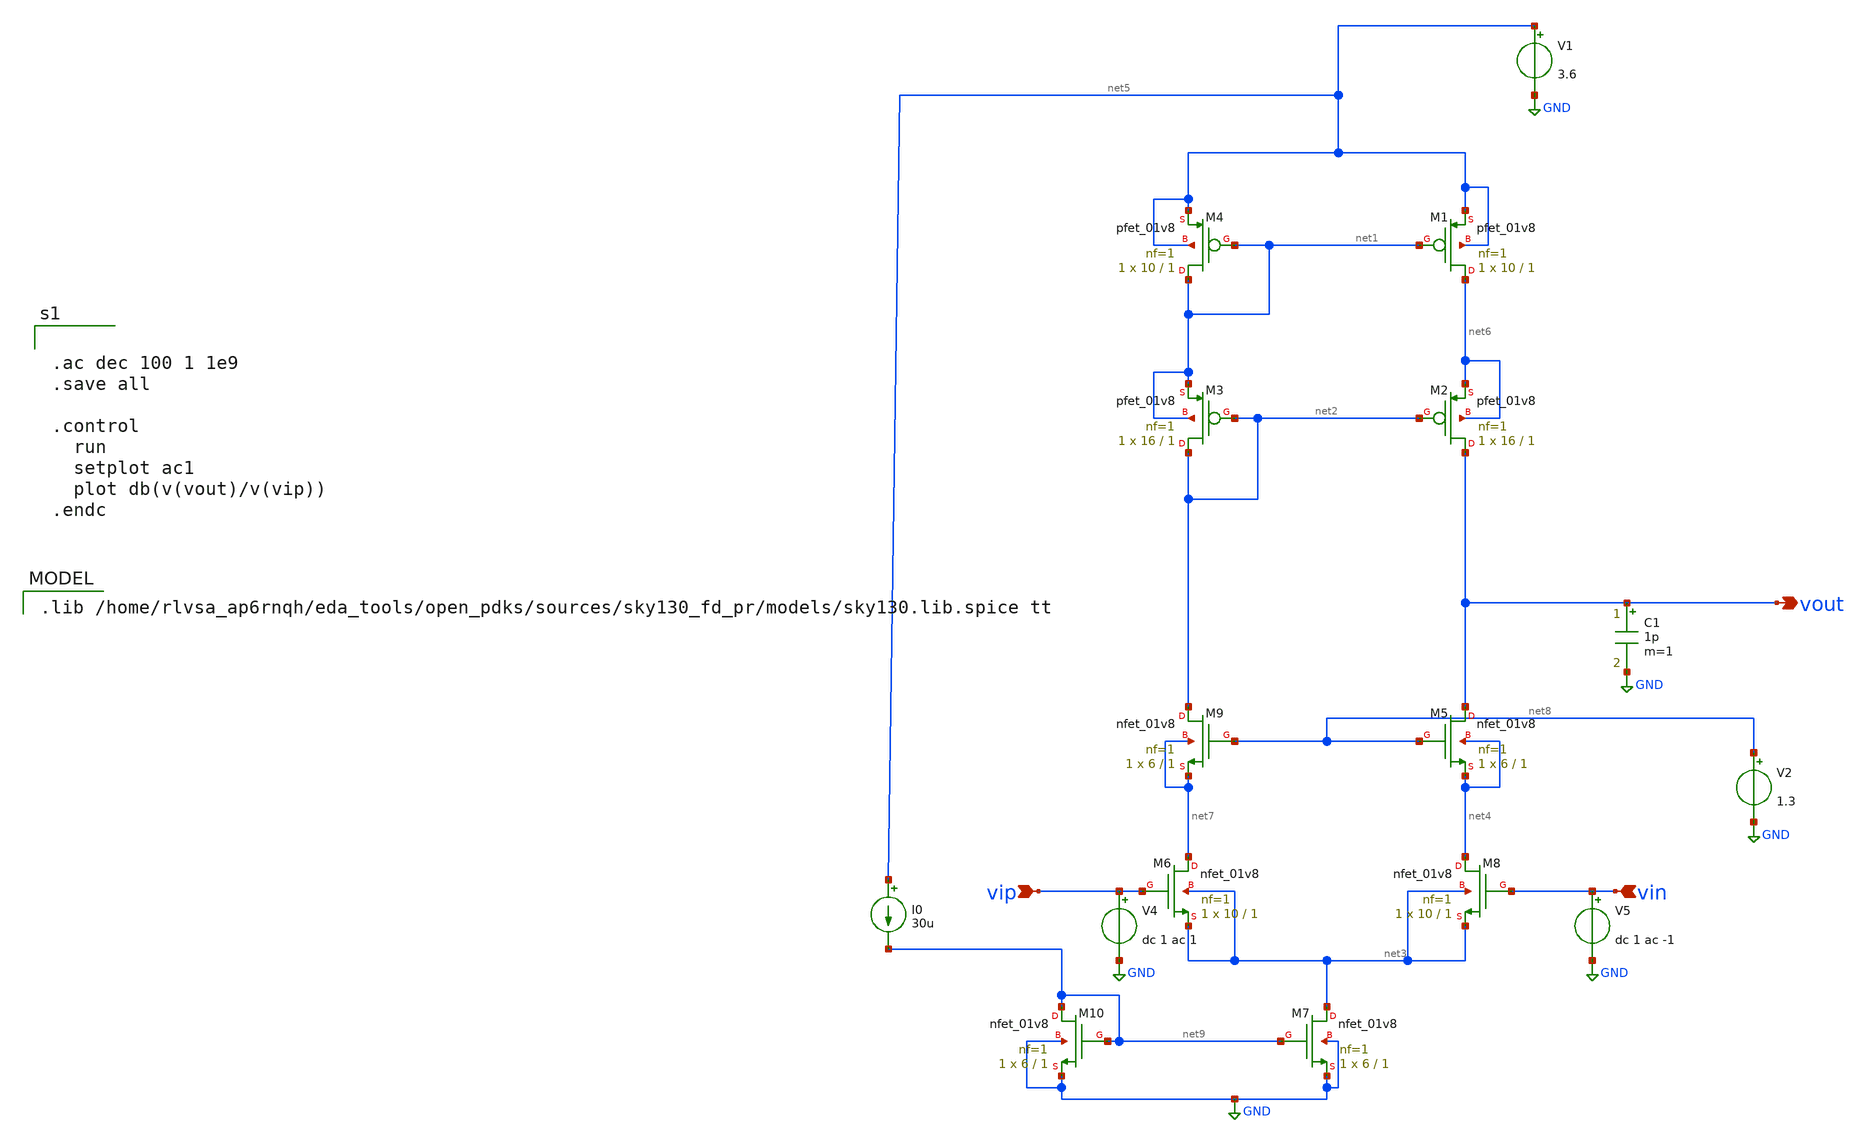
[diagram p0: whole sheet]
** sch_path: Telscopic_Opamp/9T_schematic.sch
**.subckt 9T_schematic vout vip vin
*.opin vout
*.ipin vip
*.ipin vin
V1 net5 GND 3.6
C1 vout GND 1p m=1
V2 net8 GND 1.3
V4 vip GND dc 1 ac 1
V5 vin GND dc 1 ac -1
I0 net5 net9 30u
XM5 vout net8 net4 net4 sky130_fd_pr__nfet_01v8 L=1 W=6 nf=1 ad='int((1 + 1)/2) * 6 / 1 * 0.29' as='int((1 + 2)/2) * 6 / 1 * 0.29'
+ pd='2*int((1 + 1)/2) * (6 / 1 + 0.29)' ps='2*int((1 + 2)/2) * (6 / 1 + 0.29)' nrd='0.29 / 6 ' nrs='0.29 / 6 '
+ sa=0 sb=0 sd=0 mult=1 m=1
XM6 net7 vip net3 net3 sky130_fd_pr__nfet_01v8 L=1 W=10 nf=1 ad='int((1 + 1)/2) * 10 / 1 * 0.29' as='int((1 + 2)/2) * 10 / 1 * 0.29'
+ pd='2*int((1 + 1)/2) * (10 / 1 + 0.29)' ps='2*int((1 + 2)/2) * (10 / 1 + 0.29)' nrd='0.29 / 10 ' nrs='0.29 / 10 '
+ sa=0 sb=0 sd=0 mult=1 m=1
XM7 net3 net9 GND GND sky130_fd_pr__nfet_01v8 L=1 W=6 nf=1 ad='int((1 + 1)/2) * 6 / 1 * 0.29' as='int((1 + 2)/2) * 6 / 1 * 0.29'
+ pd='2*int((1 + 1)/2) * (6 / 1 + 0.29)' ps='2*int((1 + 2)/2) * (6 / 1 + 0.29)' nrd='0.29 / 6 ' nrs='0.29 / 6 '
+ sa=0 sb=0 sd=0 mult=1 m=1
XM8 net4 vin net3 net3 sky130_fd_pr__nfet_01v8 L=1 W=10 nf=1 ad='int((1 + 1)/2) * 10 / 1 * 0.29' as='int((1 + 2)/2) * 10 / 1 * 0.29'
+ pd='2*int((1 + 1)/2) * (10 / 1 + 0.29)' ps='2*int((1 + 2)/2) * (10 / 1 + 0.29)' nrd='0.29 / 10 ' nrs='0.29 / 10 '
+ sa=0 sb=0 sd=0 mult=1 m=1
XM9 net2 net8 net7 net7 sky130_fd_pr__nfet_01v8 L=1 W=6 nf=1 ad='int((1 + 1)/2) * 6 / 1 * 0.29' as='int((1 + 2)/2) * 6 / 1 * 0.29'
+ pd='2*int((1 + 1)/2) * (6 / 1 + 0.29)' ps='2*int((1 + 2)/2) * (6 / 1 + 0.29)' nrd='0.29 / 6 ' nrs='0.29 / 6 '
+ sa=0 sb=0 sd=0 mult=1 m=1
XM10 net9 net9 GND GND sky130_fd_pr__nfet_01v8 L=1 W=6 nf=1 ad='int((1 + 1)/2) * 6 / 1 * 0.29' as='int((1 + 2)/2) * 6 / 1 * 0.29'
+ pd='2*int((1 + 1)/2) * (6 / 1 + 0.29)' ps='2*int((1 + 2)/2) * (6 / 1 + 0.29)' nrd='0.29 / 6 ' nrs='0.29 / 6 '
+ sa=0 sb=0 sd=0 mult=1 m=1
XM1 net6 net1 net5 net5 sky130_fd_pr__pfet_01v8 L=1 W=10 nf=1 ad='int((1 + 1)/2) * 10 / 1 * 0.29' as='int((1 + 2)/2) * 10 / 1 * 0.29'
+ pd='2*int((1 + 1)/2) * (10 / 1 + 0.29)' ps='2*int((1 + 2)/2) * (10 / 1 + 0.29)' nrd='0.29 / 10 ' nrs='0.29 / 10 '
+ sa=0 sb=0 sd=0 mult=1 m=1
XM2 vout net2 net6 net6 sky130_fd_pr__pfet_01v8 L=1 W=16 nf=1 ad='int((1 + 1)/2) * 16 / 1 * 0.29' as='int((1 + 2)/2) * 16 / 1 * 0.29'
+ pd='2*int((1 + 1)/2) * (16 / 1 + 0.29)' ps='2*int((1 + 2)/2) * (16 / 1 + 0.29)' nrd='0.29 / 16 ' nrs='0.29 / 16 '
+ sa=0 sb=0 sd=0 mult=1 m=1
XM3 net2 net2 net1 net1 sky130_fd_pr__pfet_01v8 L=1 W=16 nf=1 ad='int((1 + 1)/2) * 16 / 1 * 0.29' as='int((1 + 2)/2) * 16 / 1 * 0.29'
+ pd='2*int((1 + 1)/2) * (16 / 1 + 0.29)' ps='2*int((1 + 2)/2) * (16 / 1 + 0.29)' nrd='0.29 / 16 ' nrs='0.29 / 16 '
+ sa=0 sb=0 sd=0 mult=1 m=1
XM4 net1 net1 net5 net5 sky130_fd_pr__pfet_01v8 L=1 W=10 nf=1 ad='int((1 + 1)/2) * 10 / 1 * 0.29' as='int((1 + 2)/2) * 10 / 1 * 0.29'
+ pd='2*int((1 + 1)/2) * (10 / 1 + 0.29)' ps='2*int((1 + 2)/2) * (10 / 1 + 0.29)' nrd='0.29 / 10 ' nrs='0.29 / 10 '
+ sa=0 sb=0 sd=0 mult=1 m=1
**** begin user architecture code


.ac dec 100 1 1e9
.save all

.control
  run
  setplot ac1
  plot db(v(vout)/v(vip))
.endc


.lib /home/rlvsa_ap6rnqh/eda_tools/open_pdks/sources/sky130_fd_pr/models/sky130.lib.spice tt

**** end user architecture code
**.ends
.GLOBAL GND
.end
